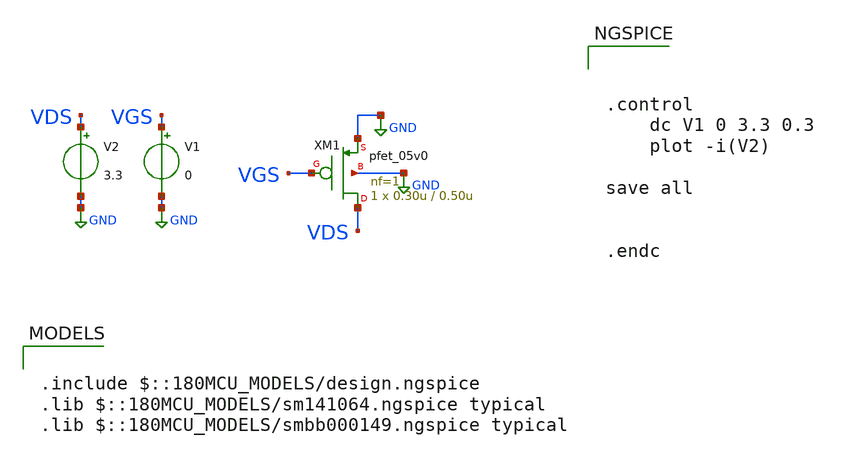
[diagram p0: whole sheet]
** sch_path: week01_mosfet_cmos/tugas1_iv_curve/mosfet-iv-characteristics-pmos.sch
**.subckt mosfet-iv-characteristics-pmos
V1 VGS GND 0
V2 VDS GND 3.3
XM1 VDS VGS GND GND pfet_05v0 L=0.50u W=0.30u nf=1 ad='int((nf+1)/2) * W/nf * 0.18u' as='int((nf+2)/2) * W/nf * 0.18u'
+ pd='2*int((nf+1)/2) * (W/nf + 0.18u)' ps='2*int((nf+2)/2) * (W/nf + 0.18u)' nrd='0.18u / W' nrs='0.18u / W'
+ sa=0 sb=0 sd=0 m=1
**** begin user architecture code

.include $::180MCU_MODELS/design.ngspice
.lib $::180MCU_MODELS/sm141064.ngspice typical
.lib $::180MCU_MODELS/smbb000149.ngspice typical




.control
	dc V1 0 3.3 0.3
	plot -i(V2)

save all


.endc


**** end user architecture code
**.ends
.GLOBAL GND
.end
